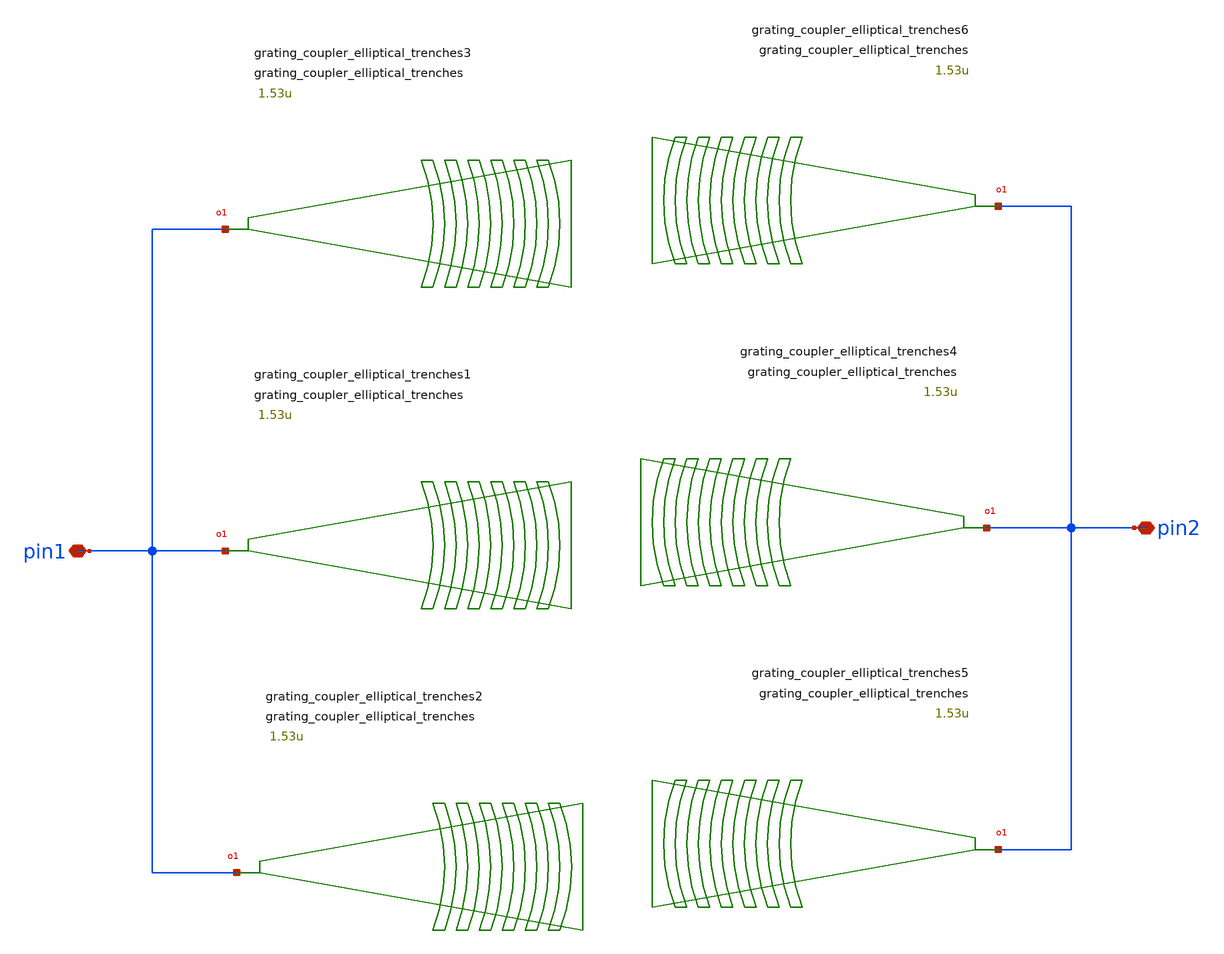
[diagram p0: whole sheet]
** sch_path: xschem/tests/test_sch/test_grating_coupler_elliptical_trenches.sch
* Copyright (c) 2024, Mabrains LLC
* Licensed under the GNU Lesser General Public License, Version 3.0 (the "License");
* you may not use this file except in compliance with the License.
* GNU Lesser General Public License
* Version 3, 29 June 2007
* This program is free software: you can redistribute it and/or modify
* it under the terms of the GNU Lesser General Public License as published
* by the Free Software Foundation, either version 3 of the License, or
* (at your option) any later version.
* This program is distributed in the hope that it will be useful,
* but WITHOUT ANY WARRANTY; without even the implied warranty of
* MERCHANTABILITY or FITNESS FOR A PARTICULAR PURPOSE.  See the
* GNU Lesser General Public License for more details.
* You should have received a copy of the GNU Lesser General Public License
* along with this program.  If not, see <https://www.gnu.org/licenses/>.
* SPDX-License-Identifier: LGPL-3.0
**.subckt test_grating_coupler_elliptical_trenches pin1 pin2
*.iopin pin1
*.iopin pin2
Pgrating_coupler_elliptical_trenches1 pin1 grating_coupler_elliptical_trenches taper_length=16.6u
+ taper_angle=30.0 wavelength=1.53u fiber_angle=15.0 grating_line_width=0.343u p_start=26 n_periods=30
+ end_straight_length=0.2u
Pgrating_coupler_elliptical_trenches2 pin1 grating_coupler_elliptical_trenches taper_length=16.6u
+ taper_angle=30.0 wavelength=1.53u fiber_angle=15.0 grating_line_width=0.343u p_start=26 n_periods=30
+ end_straight_length=0.2u
Pgrating_coupler_elliptical_trenches3 pin1 grating_coupler_elliptical_trenches taper_length=16.6u
+ taper_angle=30.0 wavelength=1.53u fiber_angle=15.0 grating_line_width=0.343u p_start=26 n_periods=30
+ end_straight_length=0.2u
Pgrating_coupler_elliptical_trenches4 pin2 grating_coupler_elliptical_trenches taper_length=16.6u
+ taper_angle=30.0 wavelength=1.53u fiber_angle=15.0 grating_line_width=0.343u p_start=26 n_periods=30
+ end_straight_length=0.2u
Pgrating_coupler_elliptical_trenches5 pin2 grating_coupler_elliptical_trenches taper_length=16.6u
+ taper_angle=30.0 wavelength=1.53u fiber_angle=15.0 grating_line_width=0.343u p_start=26 n_periods=30
+ end_straight_length=0.2u
Pgrating_coupler_elliptical_trenches6 pin2 grating_coupler_elliptical_trenches taper_length=16.6u
+ taper_angle=30.0 wavelength=1.53u fiber_angle=15.0 grating_line_width=0.343u p_start=26 n_periods=30
+ end_straight_length=0.2u
**.ends
.end
